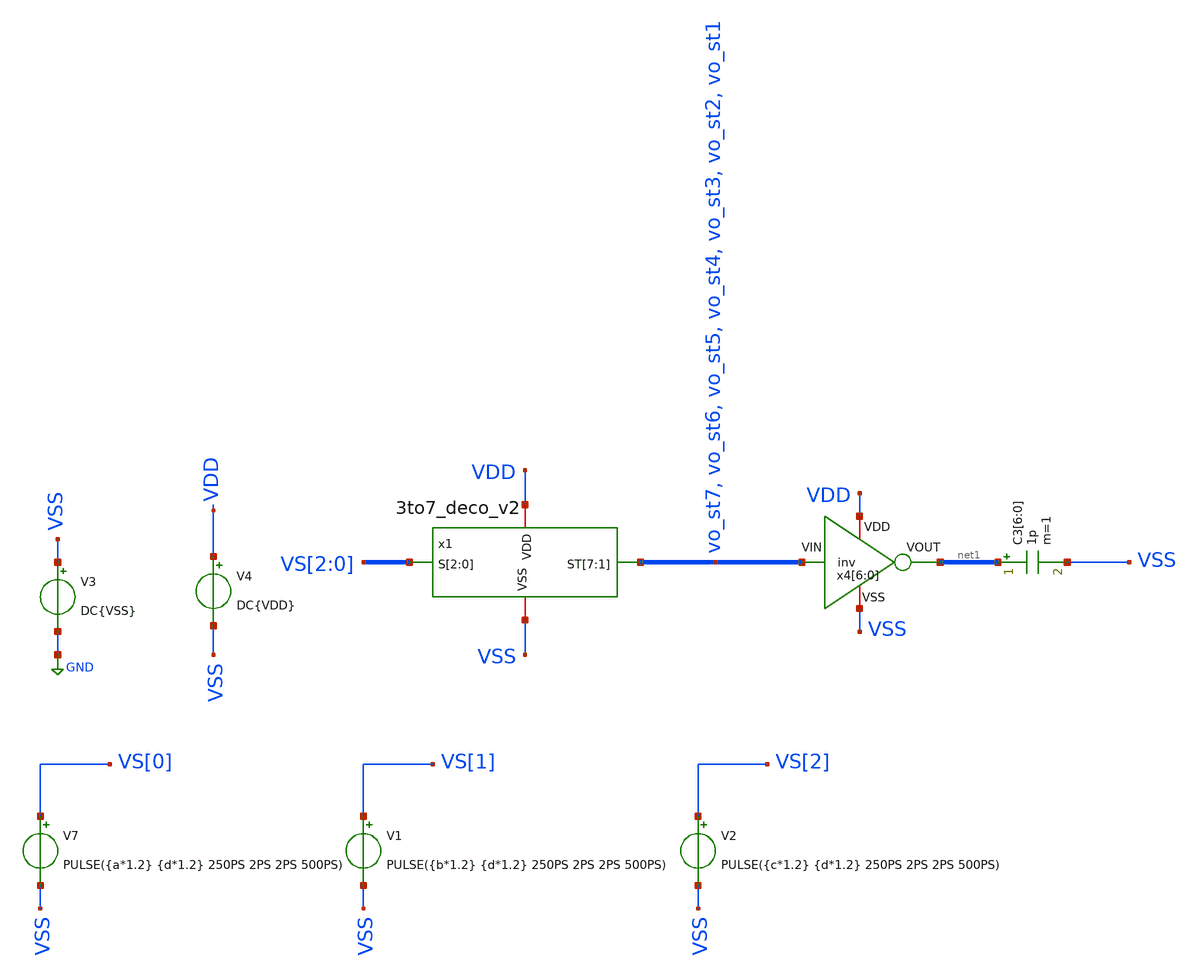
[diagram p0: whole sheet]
** sch_path: verification/testbenches/tb_3to7_deco_v2_tran.sch
**.subckt tb_3to7_deco_v2_tran
V7 VS[0] VSS PULSE({a*1.2} {d*1.2} 250PS 2PS 2PS 500PS)
V1 VS[1] VSS PULSE({b*1.2} {d*1.2} 250PS 2PS 2PS 500PS)
V2 VS[2] VSS PULSE({c*1.2} {d*1.2} 250PS 2PS 2PS 500PS)
V3 VSS GND DC{VSS}
V4 VDD VSS DC{VDD}
x4[6] VDD net1[6] vo_st7 VSS inv
x4[5] VDD net1[5] vo_st6 VSS inv
x4[4] VDD net1[4] vo_st5 VSS inv
x4[3] VDD net1[3] vo_st4 VSS inv
x4[2] VDD net1[2] vo_st3 VSS inv
x4[1] VDD net1[1] vo_st2 VSS inv
x4[0] VDD net1[0] vo_st1 VSS inv
C3[6] net1[6] VSS 1p m=1
C3[5] net1[5] VSS 1p m=1
C3[4] net1[4] VSS 1p m=1
C3[3] net1[3] VSS 1p m=1
C3[2] net1[2] VSS 1p m=1
C3[1] net1[1] VSS 1p m=1
C3[0] net1[0] VSS 1p m=1
x1 vo_st7 vo_st6 vo_st5 vo_st4 vo_st3 vo_st2 vo_st1 VS[2] VS[1] VS[0] VDD VSS 3to7_deco_v2
**** begin user architecture code



* Circuit Parameters
.param vdd = 1.2
.param vss = 0.0
.param a=0
.param b=0
.param c=0
.param d=1
.param Tclk = 500P
.options TEMP = 65.0

* Include Models
.lib /foss/pdks/ihp-sg13g2/libs.tech/ngspice/models/cornerMOSlv.lib mos_tt
cornerMOSlv.lib mos_tt
cornerMOShv.lib mos_tt
cornerHBT.lib hbt_typ
cornerRES.lib res_typ

* OP Parameters & Singals to save
.save all

*Simulations
.control
set output_path = tb_bin2thermo_tran/


* --- ESTADO 1: Entrada 001 (Salida T1 activa) ---
alterparam a=0 b=0 c=1
reset
tran 0.2PS 500PS
setplot tran1
plot vo_st7 ylabel Vout xlabel Vin
set filetype =ascii
write {$output_path}V2out1.raw V(vo_st7)

* --- ESTADO 2: Entrada 010 (Salidas T1, T2 activas) ---
alterparam a=0 b=1 c=0
reset
tran 0.2PS 500PS
setplot tran2
plot vo_st7 vo_st6 ylabel Vout xlabel Vin
set filetype =ascii
write {$output_path}V2out2.raw V(vo_st7) V(vo_st6)

* --- ESTADO 3: Entrada 011 (Salidas T1, T2, T3 activas) ---
alterparam a=0 b=1 c=1
reset
tran 0.2PS 500PS
setplot tran3
plot vo_st7 vo_st6 vo_st5 ylabel Vout xlabel Vin
set filetype =ascii
write {$output_path}V2out3.raw V(vo_st7) V(vo_st6) V(vo_st5)

* --- ESTADO 4: Entrada 100 (Salidas T1 a T4 activas) ---
alterparam a=1 b=0 c=0
reset
tran 0.2PS 500PS
setplot tran4
plot  vo_st7 vo_st6 vo_st5 vo_st4 ylabel Vout xlabel Vin
set filetype =ascii
write {$output_path}V2out4.raw V(vo_st7) V(vo_st6) V(vo_st5) V(vo_st4)

* --- ESTADO 5: Entrada 101 (Salidas T1 a T5 activas) ---
alterparam a=1 b=0 c=1
reset
tran 0.2PS 500PS
setplot tran5
plot vo_st7 vo_st6 vo_st5 vo_st4 vo_st3 ylabel Vout xlabel Vin
set filetype =ascii
write {$output_path}V2out5.raw V(vo_st7) V(vo_st6) V(vo_st5) V(vo_st4) V(vo_st3)

* --- ESTADO 6: Entrada 110 (Salidas T1 a T6 activas) ---
alterparam a=1 b=1 c=0
reset
tran 0.2PS 500PS
setplot tran6
plot vo_st7 vo_st6 vo_st5 vo_st4 vo_st3 vo_st2 ylabel Vout xlabel Vin
set filetype =ascii
write {$output_path}V2out6.raw V(vo_st7) V(vo_st6) V(vo_st5) V(vo_st4) V(vo_st3) V(vo_st2)

* --- ESTADO 7: Entrada 111 (Salidas T1 a T7 activas) ---
alterparam a=1 b=1 c=1
reset
tran 0.2PS 500PS
setplot tran7
plot vo_st7 vo_st6 vo_st5 vo_st4 vo_st3 vo_st2 vo_st1 ylabel Vout xlabel Vin
set filetype =ascii
write {$output_path}V2out7.raw V(vo_st7) V(vo_st6) V(vo_st5) V(vo_st4) V(vo_st3) V(vo_st2) V(vo_st1)
.endc
.end

**** end user architecture code
**.ends
.GLOBAL GND
.end
